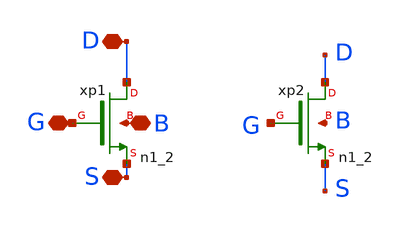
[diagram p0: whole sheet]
** sch_path: macros/comparator/schematic/xschem/n1_4.sch
**.subckt n1_4 D G S B
*.iopin D
*.iopin G
*.iopin S
*.iopin B
xp1 D G S B n1_2
xp2 D G S B n1_2
**.ends

* expanding   symbol:  n1_2.sym # of pins=4
** sym_path: macros/comparator/schematic/xschem/n1_2.sym
** sch_path: macros/comparator/schematic/xschem/n1_2.sch
.subckt n1_2 D G S B
*.iopin G
*.iopin D
*.iopin S
*.iopin B
XMbot D G X B sg13_hv_nmos w=2.5e-6 l=1e-6 ng=1 m=1 mm_ok=1
XMtop X G S B sg13_hv_nmos w=2.5e-6 l=1e-6 ng=1 m=1 mm_ok=1
.ends

.end
